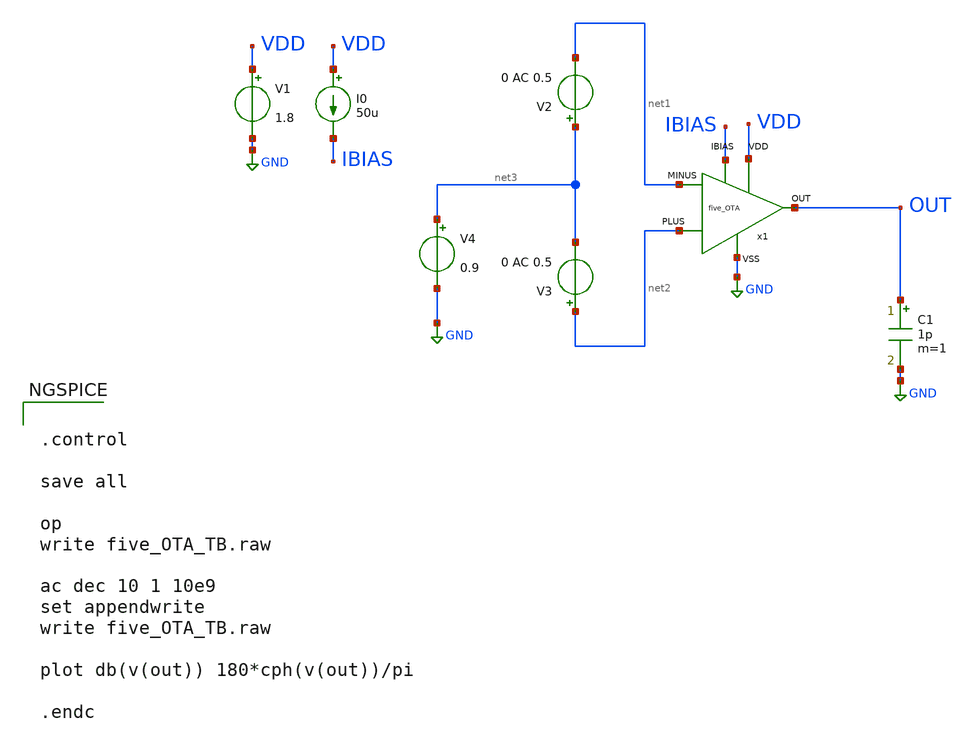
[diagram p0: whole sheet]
** sch_path: five_OTA/five_OTA_TB.sch
**.subckt five_OTA_TB
x1 net1 net2 IBIAS VDD GND OUT five_OTA
V1 VDD GND 1.8
I0 VDD IBIAS 50u
V2 net3 net1 0 AC 0.5
V3 net2 net3 0 AC 0.5
V4 net3 GND 0.9
C1 OUT GND 1p m=1
**** begin user architecture code


.control

save all

op
write five_OTA_TB.raw

ac dec 10 1 10e9
set appendwrite
write five_OTA_TB.raw

plot db(v(out)) 180*cph(v(out))/pi

.endc



** opencircuitdesign pdks install
.lib $::SKYWATER_MODELS/sky130.lib.spice tt


**** end user architecture code
**.ends

* expanding   symbol:  design/zehra-work/five_OTA.sym # of pins=6
** sym_path: five_OTA/five_OTA.sym
** sch_path: five_OTA/five_OTA.sch
.subckt five_OTA MINUS PLUS IBIAS VDD VSS OUT
*.iopin VDD
*.iopin VSS
*.iopin IBIAS
*.iopin MINUS
*.iopin PLUS
*.iopin OUT
XM4 net2 PLUS net1 VSS sky130_fd_pr__nfet_01v8_lvt L=0.3 W=4 nf=1 ad='int((nf+1)/2) * W/nf * 0.29' as='int((nf+2)/2) * W/nf * 0.29'
+ pd='2*int((nf+1)/2) * (W/nf + 0.29)' ps='2*int((nf+2)/2) * (W/nf + 0.29)' nrd='0.29 / W' nrs='0.29 / W'
+ sa=0 sb=0 sd=0 mult=4 m=4
XM5 OUT MINUS net1 VSS sky130_fd_pr__nfet_01v8_lvt L=0.3 W=4 nf=1 ad='int((nf+1)/2) * W/nf * 0.29' as='int((nf+2)/2) * W/nf * 0.29'
+ pd='2*int((nf+1)/2) * (W/nf + 0.29)' ps='2*int((nf+2)/2) * (W/nf + 0.29)' nrd='0.29 / W' nrs='0.29 / W'
+ sa=0 sb=0 sd=0 mult=4 m=4
XM1 net1 IBIAS VSS VSS sky130_fd_pr__nfet_01v8 L=0.3 W=3 nf=1 ad='int((nf+1)/2) * W/nf * 0.29' as='int((nf+2)/2) * W/nf * 0.29'
+ pd='2*int((nf+1)/2) * (W/nf + 0.29)' ps='2*int((nf+2)/2) * (W/nf + 0.29)' nrd='0.29 / W' nrs='0.29 / W'
+ sa=0 sb=0 sd=0 mult=4 m=4
XM2 IBIAS IBIAS VSS VSS sky130_fd_pr__nfet_01v8 L=0.3 W=3 nf=1 ad='int((nf+1)/2) * W/nf * 0.29' as='int((nf+2)/2) * W/nf * 0.29'
+ pd='2*int((nf+1)/2) * (W/nf + 0.29)' ps='2*int((nf+2)/2) * (W/nf + 0.29)' nrd='0.29 / W' nrs='0.29 / W'
+ sa=0 sb=0 sd=0 mult=1 m=1
XM3 net2 net2 VDD VDD sky130_fd_pr__pfet_01v8_lvt L=0.7 W=2.3 nf=1 ad='int((nf+1)/2) * W/nf * 0.29' as='int((nf+2)/2) * W/nf * 0.29'
+ pd='2*int((nf+1)/2) * (W/nf + 0.29)' ps='2*int((nf+2)/2) * (W/nf + 0.29)' nrd='0.29 / W' nrs='0.29 / W'
+ sa=0 sb=0 sd=0 mult=4 m=4
XM6 OUT net2 VDD VDD sky130_fd_pr__pfet_01v8_lvt L=0.7 W=2.3 nf=1 ad='int((nf+1)/2) * W/nf * 0.29' as='int((nf+2)/2) * W/nf * 0.29'
+ pd='2*int((nf+1)/2) * (W/nf + 0.29)' ps='2*int((nf+2)/2) * (W/nf + 0.29)' nrd='0.29 / W' nrs='0.29 / W'
+ sa=0 sb=0 sd=0 mult=4 m=4
.save v(net2)
.save v(ibias)
.save v(net1)
.save v(out)
.ends

.GLOBAL GND
.end
